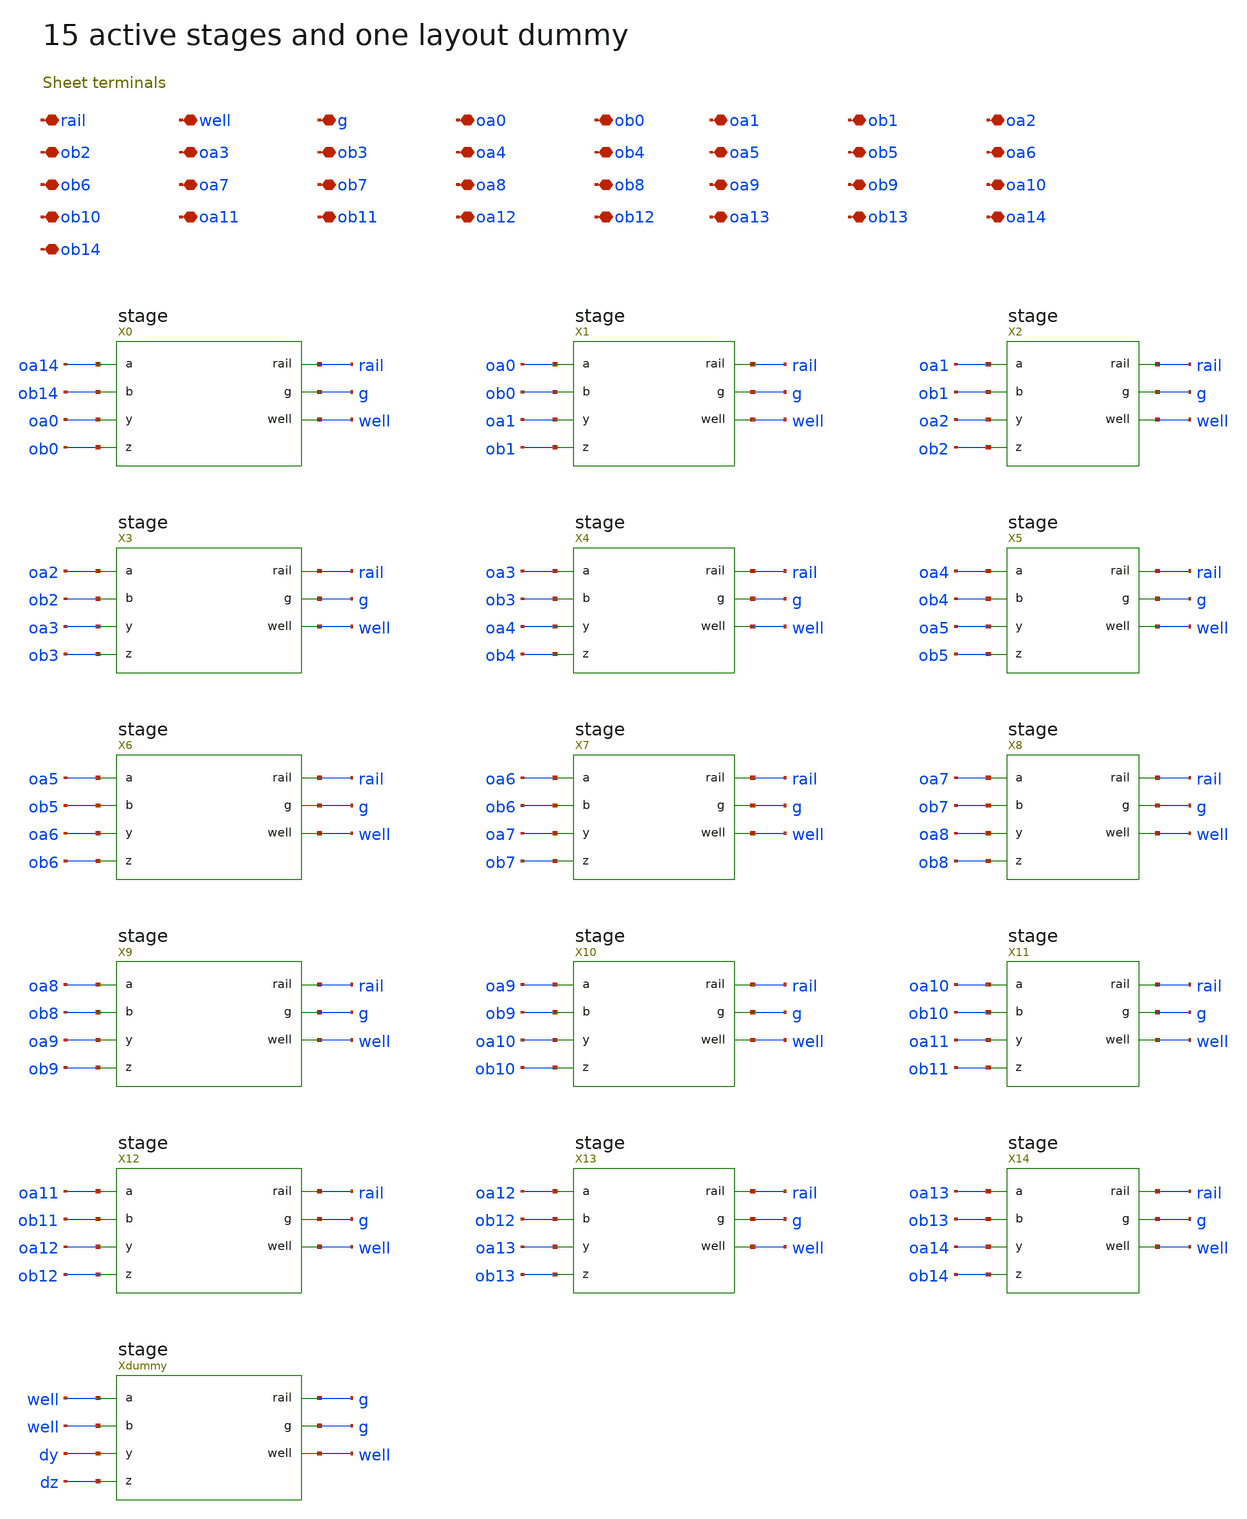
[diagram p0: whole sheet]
** sch_path: review/xschem/bank.sch
**.subckt bank rail well g oa0 ob0 oa1 ob1 oa2 ob2 oa3 ob3 oa4 ob4 oa5 ob5 oa6 ob6 oa7 ob7 oa8 ob8
*+ oa9 ob9 oa10 ob10 oa11 ob11 oa12 ob12 oa13 ob13 oa14 ob14
*.iopin rail
*.iopin well
*.iopin g
*.iopin oa0
*.iopin ob0
*.iopin oa1
*.iopin ob1
*.iopin oa2
*.iopin ob2
*.iopin oa3
*.iopin ob3
*.iopin oa4
*.iopin ob4
*.iopin oa5
*.iopin ob5
*.iopin oa6
*.iopin ob6
*.iopin oa7
*.iopin ob7
*.iopin oa8
*.iopin ob8
*.iopin oa9
*.iopin ob9
*.iopin oa10
*.iopin ob10
*.iopin oa11
*.iopin ob11
*.iopin oa12
*.iopin ob12
*.iopin oa13
*.iopin ob13
*.iopin oa14
*.iopin ob14
X0 oa14 ob14 oa0 ob0 rail g well stage
X1 oa0 ob0 oa1 ob1 rail g well stage
X2 oa1 ob1 oa2 ob2 rail g well stage
X3 oa2 ob2 oa3 ob3 rail g well stage
X4 oa3 ob3 oa4 ob4 rail g well stage
X5 oa4 ob4 oa5 ob5 rail g well stage
X6 oa5 ob5 oa6 ob6 rail g well stage
X7 oa6 ob6 oa7 ob7 rail g well stage
X8 oa7 ob7 oa8 ob8 rail g well stage
X9 oa8 ob8 oa9 ob9 rail g well stage
X10 oa9 ob9 oa10 ob10 rail g well stage
X11 oa10 ob10 oa11 ob11 rail g well stage
X12 oa11 ob11 oa12 ob12 rail g well stage
X13 oa12 ob12 oa13 ob13 rail g well stage
X14 oa13 ob13 oa14 ob14 rail g well stage
Xdummy well well dy dz g g well stage
**.ends

* expanding   symbol:  stage.sym # of pins=7
** sym_path: review/xschem/stage.sym
** sch_path: review/xschem/stage.sch
.subckt stage a b y z rail g well
*.iopin a
*.iopin b
*.iopin y
*.iopin z
*.iopin rail
*.iopin g
*.iopin well
XCca g y sky130_fd_pr__cap_mim_m3_1 W=4.5 L=4.5 MF=1 m=1
XCcb g z sky130_fd_pr__cap_mim_m3_1 W=4.5 L=4.5 MF=1 m=1
XMmainA_Xp y a rail well sky130_fd_pr__pfet_01v8_lvt L=.55 W=8.4 nf=1 ad='int((1 + 1)/2) * 8.4 / 1 * 0.29'
+ as='int((1 + 2)/2) * 8.4 / 1 * 0.29' pd='2*int((1 + 1)/2) * (8.4 / 1 + 0.29)' ps='2*int((1 + 2)/2) * (8.4 / 1 + 0.29)'
+ nrd='0.29 / 8.4 ' nrs='0.29 / 8.4 ' sa=0 sb=0 sd=0 mult=1 m=1
XMmainA_Xn y a g g sky130_fd_pr__nfet_01v8 L=.55 W=4.2 nf=1 ad='int((1 + 1)/2) * 4.2 / 1 * 0.29' as='int((1 + 2)/2) * 4.2 / 1 * 0.29'
+ pd='2*int((1 + 1)/2) * (4.2 / 1 + 0.29)' ps='2*int((1 + 2)/2) * (4.2 / 1 + 0.29)' nrd='0.29 / 4.2 ' nrs='0.29 / 4.2 '
+ sa=0 sb=0 sd=0 mult=1 m=1
XMmainB_Xp z b rail well sky130_fd_pr__pfet_01v8_lvt L=.55 W=8.4 nf=1 ad='int((1 + 1)/2) * 8.4 / 1 * 0.29'
+ as='int((1 + 2)/2) * 8.4 / 1 * 0.29' pd='2*int((1 + 1)/2) * (8.4 / 1 + 0.29)' ps='2*int((1 + 2)/2) * (8.4 / 1 + 0.29)'
+ nrd='0.29 / 8.4 ' nrs='0.29 / 8.4 ' sa=0 sb=0 sd=0 mult=1 m=1
XMmainB_Xn z b g g sky130_fd_pr__nfet_01v8 L=.55 W=4.2 nf=1 ad='int((1 + 1)/2) * 4.2 / 1 * 0.29' as='int((1 + 2)/2) * 4.2 / 1 * 0.29'
+ pd='2*int((1 + 1)/2) * (4.2 / 1 + 0.29)' ps='2*int((1 + 2)/2) * (4.2 / 1 + 0.29)' nrd='0.29 / 4.2 ' nrs='0.29 / 4.2 '
+ sa=0 sb=0 sd=0 mult=1 m=1
XMcrossA_Xp z y rail well sky130_fd_pr__pfet_01v8_lvt L=.55 W=1.68 nf=1 ad='int((1 + 1)/2) * 1.68 / 1 * 0.29'
+ as='int((1 + 2)/2) * 1.68 / 1 * 0.29' pd='2*int((1 + 1)/2) * (1.68 / 1 + 0.29)' ps='2*int((1 + 2)/2) * (1.68 / 1 + 0.29)'
+ nrd='0.29 / 1.68 ' nrs='0.29 / 1.68 ' sa=0 sb=0 sd=0 mult=1 m=1
XMcrossA_Xn z y g g sky130_fd_pr__nfet_01v8 L=.55 W=.84 nf=1 ad='int((1 + 1)/2) * .84 / 1 * 0.29' as='int((1 + 2)/2) * .84 / 1 * 0.29'
+ pd='2*int((1 + 1)/2) * (.84 / 1 + 0.29)' ps='2*int((1 + 2)/2) * (.84 / 1 + 0.29)' nrd='0.29 / .84 ' nrs='0.29 / .84 '
+ sa=0 sb=0 sd=0 mult=1 m=1
XMcrossB_Xp y z rail well sky130_fd_pr__pfet_01v8_lvt L=.55 W=1.68 nf=1 ad='int((1 + 1)/2) * 1.68 / 1 * 0.29'
+ as='int((1 + 2)/2) * 1.68 / 1 * 0.29' pd='2*int((1 + 1)/2) * (1.68 / 1 + 0.29)' ps='2*int((1 + 2)/2) * (1.68 / 1 + 0.29)'
+ nrd='0.29 / 1.68 ' nrs='0.29 / 1.68 ' sa=0 sb=0 sd=0 mult=1 m=1
XMcrossB_Xn y z g g sky130_fd_pr__nfet_01v8 L=.55 W=.84 nf=1 ad='int((1 + 1)/2) * .84 / 1 * 0.29' as='int((1 + 2)/2) * .84 / 1 * 0.29'
+ pd='2*int((1 + 1)/2) * (.84 / 1 + 0.29)' ps='2*int((1 + 2)/2) * (.84 / 1 + 0.29)' nrd='0.29 / .84 ' nrs='0.29 / .84 '
+ sa=0 sb=0 sd=0 mult=1 m=1
.ends

.end
